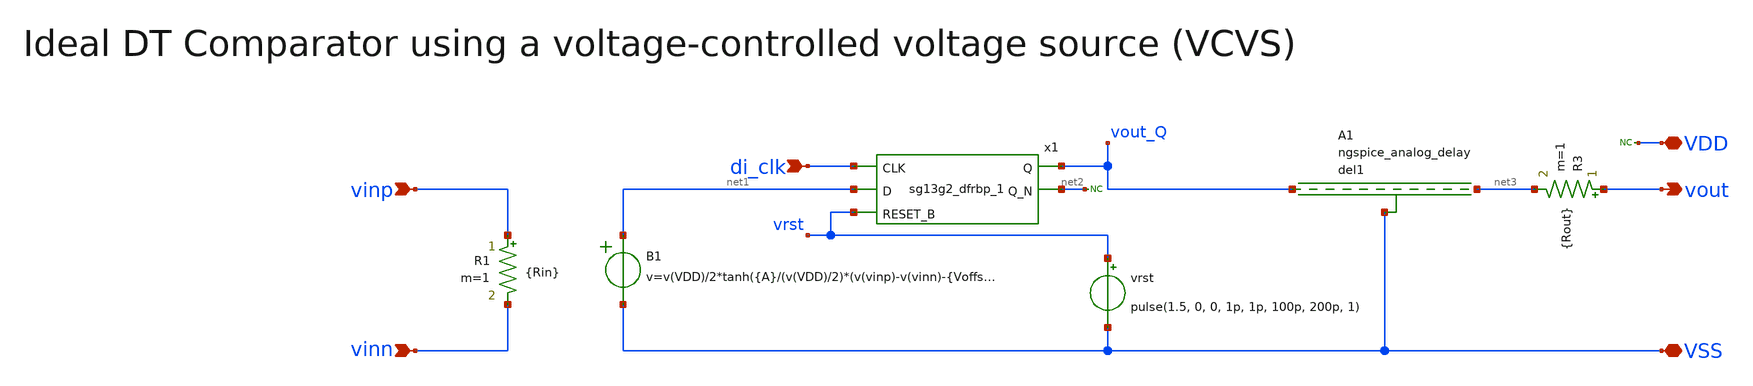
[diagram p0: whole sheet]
** sch_path: SG13G2_ATBS-ADC-main/xschem/comparator/discrete_time/ideal/DT_comparator_ideal.sch
**.subckt DT_comparator_ideal vinn vout vinp VSS VDD di_clk
*.ipin vinn
*.opin vout
*.ipin vinp
*.iopin VSS
*.iopin VDD
*.ipin di_clk
R1 vinp vinn {Rin} m=1
B1 net1 VSS v=v(VDD)/2*tanh({A}/(v(VDD)/2)*(v(vinp)-v(vinn)-{Voffs}))+{Vcm}
R3 vout net3 {Rout} m=1
* noconn #net2
vrst vrst VSS pulse(1.5, 0, 0, 1p, 1p, 100p, 200p, 1)
* noconn VDD
x1 vout_Q net2 di_clk net1 vrst VDD VSS sg13g2_dfrbp_1
A1 vout_Q net3 VSS del_subckt
.model del_subckt delay(delay=tpd buffer_size=8192)
**.ends

* expanding   symbol:  sg13g2_stdcells/sg13g2_dfrbp_1.sym # of pins=5
** sym_path: sg13g2_stdcells/sg13g2_dfrbp_1.sym
** sch_path: sg13g2_stdcells/sg13g2_dfrbp_1.sch
.subckt sg13g2_dfrbp_1 Q Q_N CLK D RESET_B VDD VSS
*.ipin D
*.ipin RESET_B
*.ipin CLK
*.opin Q
*.opin Q_N
*.iopin VDD
*.iopin VSS
XM1 Db D net10 VSS sg13_lv_nmos w=420.00n l=130.00n ng=1 m=1 mm_ok=1
XM2 net10 RESET_B VSS VSS sg13_lv_nmos w=420.00n l=130.00n ng=1 m=1 mm_ok=1
XM3 net1 clkneg net9 VSS sg13_lv_nmos w=420.00n l=130.00n ng=1 m=1 mm_ok=1
XM4 net9 net1 VSS VSS sg13_lv_nmos w=420.00n l=130.00n ng=1 m=1 mm_ok=1
XM5 net1 net1 net5 VSS sg13_lv_nmos w=420.00n l=130.00n ng=1 m=1 mm_ok=1
XM6 net5 RESET_B VSS VSS sg13_lv_nmos w=420.00n l=130.00n ng=1 m=1 mm_ok=1
XM7 Q_N net1 VSS VSS sg13_lv_nmos w=740.00n l=130.00n ng=1 m=1 mm_ok=1
XM8 net2 net1 VSS VSS sg13_lv_nmos w=740.00n l=130.00n ng=1 m=1 mm_ok=1
XM9 Q net2 VSS VSS sg13_lv_nmos w=740.00n l=130.00n ng=1 m=1 mm_ok=1
XM10 clkneg CLK VSS VSS sg13_lv_nmos w=740.00n l=130.00n ng=1 m=1 mm_ok=1
XM11 clkpos clkneg VSS VSS sg13_lv_nmos w=740.00n l=130.00n ng=1 m=1 mm_ok=1
XM12 Db clkneg net3 VSS sg13_lv_nmos w=420.00n l=130.00n ng=1 m=1 mm_ok=1
XM13 net3 clkpos net8 VSS sg13_lv_nmos w=420.00n l=130.00n ng=1 m=1 mm_ok=1
XM14 net8 net3 net4 VSS sg13_lv_nmos w=420.00n l=130.00n ng=1 m=1 mm_ok=1
XM15 net4 RESET_B VSS VSS sg13_lv_nmos w=420.00n l=130.00n ng=1 m=1 mm_ok=1
XM16 net3 net3 VSS VSS sg13_lv_nmos w=740.00n l=130.00n ng=1 m=1 mm_ok=1
XM17 net3 clkpos net1 VSS sg13_lv_nmos w=740.00n l=130.00n ng=1 m=1 mm_ok=1
XM18 Db RESET_B VDD VDD sg13_lv_pmos w=420.00n l=130.00n ng=1 m=1 mm_ok=1
XM19 Db D VDD VDD sg13_lv_pmos w=420.00n l=130.00n ng=1 m=1 mm_ok=1
XM20 net7 net1 VDD VDD sg13_lv_pmos w=420.00n l=130.00n ng=1 m=1 mm_ok=1
XM21 net1 clkpos net7 VDD sg13_lv_pmos w=420.00n l=130.00n ng=1 m=1 mm_ok=1
XM22 net1 net1 VDD VDD sg13_lv_pmos w=420.00n l=130.00n ng=1 m=1 mm_ok=1
XM23 net1 RESET_B VDD VDD sg13_lv_pmos w=420.00n l=130.00n ng=1 m=1 mm_ok=1
XM24 Q_N net1 VDD VDD sg13_lv_pmos w=1.12u l=130.00n ng=1 m=1 mm_ok=1
XM25 net2 net1 VDD VDD sg13_lv_pmos w=1.12u l=130.00n ng=1 m=1 mm_ok=1
XM26 Q net2 VDD VDD sg13_lv_pmos w=1.12u l=130.00n ng=1 m=1 mm_ok=1
XM27 clkneg CLK VDD VDD sg13_lv_pmos w=1.12u l=130.00n ng=1 m=1 mm_ok=1
XM28 clkpos clkneg VDD VDD sg13_lv_pmos w=1.12u l=130.00n ng=1 m=1 mm_ok=1
XM29 Db clkpos net3 VDD sg13_lv_pmos w=420.00n l=130.00n ng=1 m=1 mm_ok=1
XM30 net6 net3 VDD VDD sg13_lv_pmos w=420.00n l=130.00n ng=1 m=1 mm_ok=1
XM31 net3 clkneg net6 VDD sg13_lv_pmos w=420.00n l=130.00n ng=1 m=1 mm_ok=1
XM32 net3 RESET_B VDD VDD sg13_lv_pmos w=420.00n l=130.00n ng=1 m=1 mm_ok=1
XM33 net3 net3 VDD VDD sg13_lv_pmos w=1.000u l=130.00n ng=1 m=1 mm_ok=1
XM34 net3 clkneg net1 VDD sg13_lv_pmos w=1.000u l=130.00n ng=1 m=1 mm_ok=1
.ends

.end
